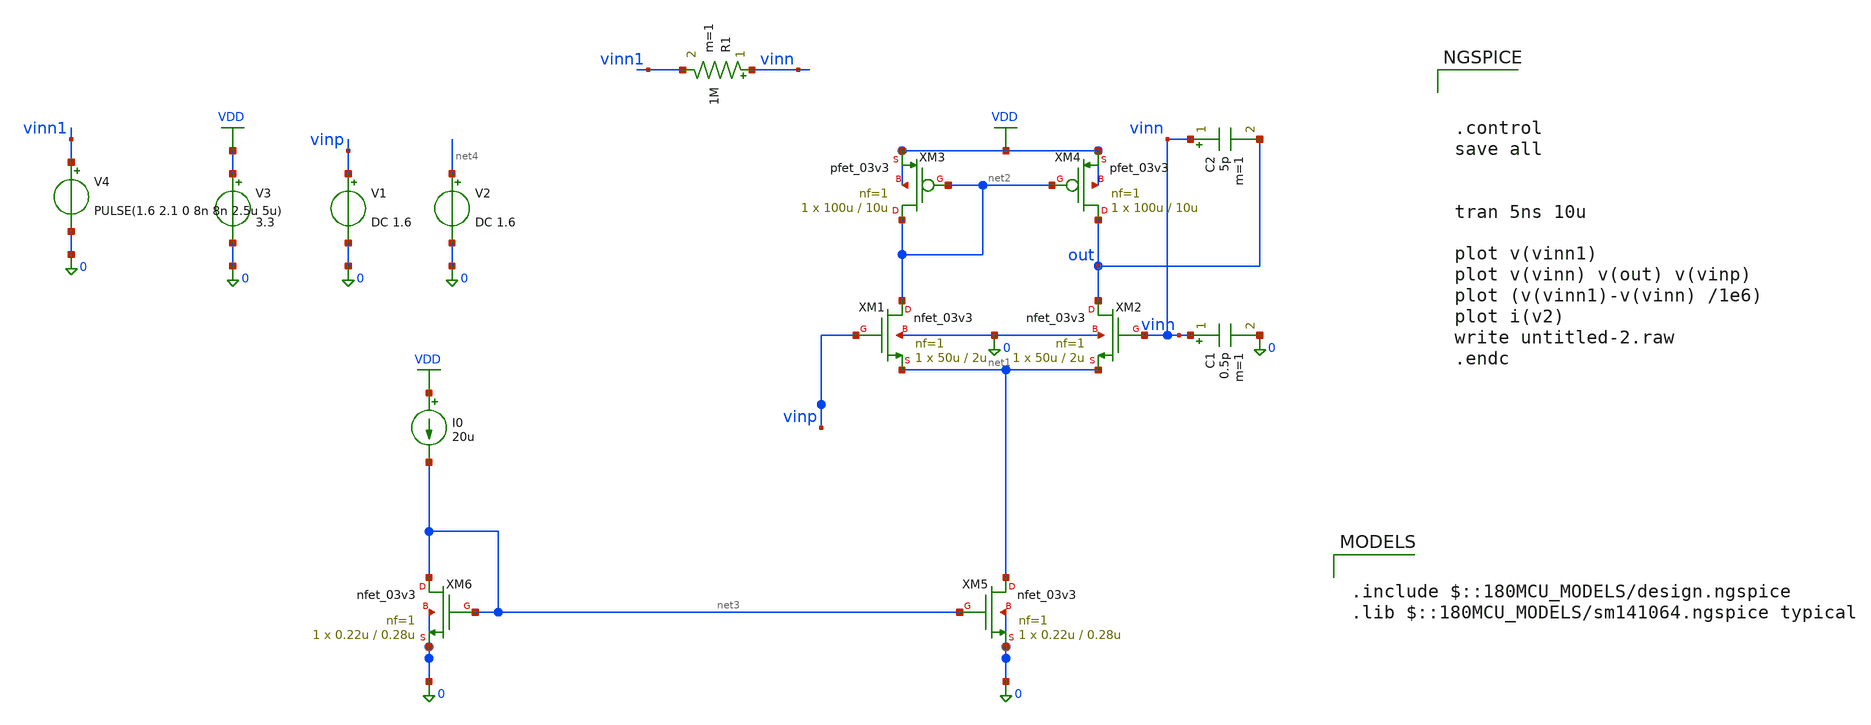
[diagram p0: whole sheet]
** sch_path: amplifier/untitled-2.sch
**.subckt untitled-2
XM1 net2 vinp net1 0 nfet_03v3 L=2u W=50u nf=1 ad='int((nf+1)/2) * W/nf * 0.18u' as='int((nf+2)/2) * W/nf * 0.18u'
+ pd='2*int((nf+1)/2) * (W/nf + 0.18u)' ps='2*int((nf+2)/2) * (W/nf + 0.18u)' nrd='0.18u / W' nrs='0.18u / W'
+ sa=0 sb=0 sd=0 m=1
XM2 out vinn net1 0 nfet_03v3 L=2u W=50u nf=1 ad='int((nf+1)/2) * W/nf * 0.18u' as='int((nf+2)/2) * W/nf * 0.18u'
+ pd='2*int((nf+1)/2) * (W/nf + 0.18u)' ps='2*int((nf+2)/2) * (W/nf + 0.18u)' nrd='0.18u / W' nrs='0.18u / W'
+ sa=0 sb=0 sd=0 m=1
XM3 net2 net2 VDD VDD pfet_03v3 L=10u W=100u nf=1 ad='int((nf+1)/2) * W/nf * 0.18u' as='int((nf+2)/2) * W/nf * 0.18u'
+ pd='2*int((nf+1)/2) * (W/nf + 0.18u)' ps='2*int((nf+2)/2) * (W/nf + 0.18u)' nrd='0.18u / W' nrs='0.18u / W'
+ sa=0 sb=0 sd=0 m=1
XM4 out net2 VDD VDD pfet_03v3 L=10u W=100u nf=1 ad='int((nf+1)/2) * W/nf * 0.18u' as='int((nf+2)/2) * W/nf * 0.18u'
+ pd='2*int((nf+1)/2) * (W/nf + 0.18u)' ps='2*int((nf+2)/2) * (W/nf + 0.18u)' nrd='0.18u / W' nrs='0.18u / W'
+ sa=0 sb=0 sd=0 m=1
XM5 net1 net3 0 0 nfet_03v3 L=0.28u W=0.22u nf=1 ad='int((nf+1)/2) * W/nf * 0.18u' as='int((nf+2)/2) * W/nf * 0.18u'
+ pd='2*int((nf+1)/2) * (W/nf + 0.18u)' ps='2*int((nf+2)/2) * (W/nf + 0.18u)' nrd='0.18u / W' nrs='0.18u / W'
+ sa=0 sb=0 sd=0 m=1
XM6 net3 net3 0 0 nfet_03v3 L=0.28u W=0.22u nf=1 ad='int((nf+1)/2) * W/nf * 0.18u' as='int((nf+2)/2) * W/nf * 0.18u'
+ pd='2*int((nf+1)/2) * (W/nf + 0.18u)' ps='2*int((nf+2)/2) * (W/nf + 0.18u)' nrd='0.18u / W' nrs='0.18u / W'
+ sa=0 sb=0 sd=0 m=1
V1 vinp 0 DC 1.6
V2 net4 0 DC 1.6
V3 VDD 0 3.3
I0 VDD net3 20u
C2 vinn out 5p m=1
R1 vinn vinn1 1M m=1
V4 vinn1 0 PULSE(1.6 2.1 0 8n 8n 2.5u 5u)
C1 vinn 0 0.5p m=1
**** begin user architecture code

.include $::180MCU_MODELS/design.ngspice
.lib $::180MCU_MODELS/sm141064.ngspice typical




.control
save all


tran 5ns 10u

plot v(vinn1)
plot v(vinn) v(out) v(vinp)
plot (v(vinn1)-v(vinn) /1e6)
plot i(v2)
write untitled-2.raw
.endc


**** end user architecture code
**.ends
.GLOBAL VDD
.end
